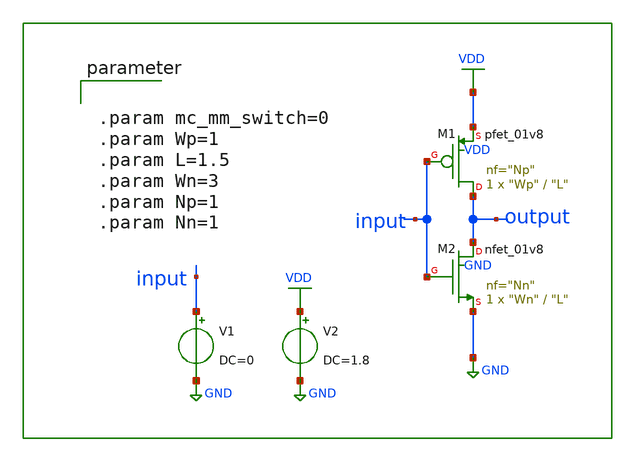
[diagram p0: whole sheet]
** sch_path: circuit_model/tb/inv_1.sch
**.subckt inv_1
XM1 output input VDD VDD sky130_fd_pr__pfet_01v8 L="L" W="Wp" nf="Np" ad='int(("Np" + 1)/2) * "Wp" / "Np" * 0.29'
+ as='int(("Np" + 2)/2) * "Wp" / "Np" * 0.29' pd='2*int(("Np" + 1)/2) * ("Wp" / "Np" + 0.29)' ps='2*int(("Np" + 2)/2) * ("Wp" / "Np" + 0.29)'
+ nrd='0.29 / "Wp" ' nrs='0.29 / "Wp" ' sa=0 sb=0 sd=0 mult=1 m=1
XM2 output input GND GND sky130_fd_pr__nfet_01v8 L="L" W="Wn" nf="Nn" ad='int((nf+1)/2) * W/nf * 0.29'
+ as='int((nf+2)/2) * W/nf * 0.29' pd='2*int((nf+1)/2) * (W/nf + 0.29)' ps='2*int((nf+2)/2) * (W/nf + 0.29)'
+ nrd='0.29 / W' nrs='0.29 / W' sa=0 sb=0 sd=0 mult=1 m=1
V1 input GND DC=0
V2 VDD GND DC=1.8
**** begin user architecture code


.lib /home/dkits/efabless/mpw-5/pdks/sky130A/libs.tech/ngspice/sky130.lib.spice tt
.inc /home/dkits/efabless/mpw-5/pdks/sky130A/libs.ref/sky130_fd_sc_hd/spice/sky130_fd_sc_hd.spice




.param mc_mm_switch=0
.param Wp=1
.param L=1.5
.param Wn=3
.param Np=1
.param Nn=1




.control
set nobreak
set numthread=11
TRAN 1n 6u
save i(M1)
save i(M2)
plot input output
.endc


**** end user architecture code
**.ends
.GLOBAL VDD
.GLOBAL GND
.end
